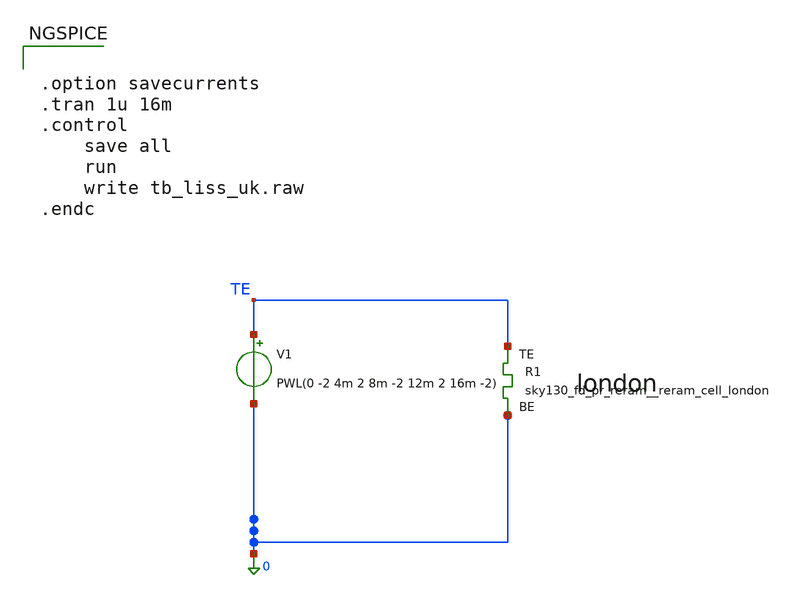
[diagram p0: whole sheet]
** sch_path: memristor_models/rram_london/tb_liss_uk.sch
**.subckt tb_liss_uk
V1 TE 0 PWL(0 -2 4m 2 8m -2 12m 2 16m -2)
XR1 TE 0 sky130_fd_pr_reram__reram_cell_london
**** begin user architecture code

** opencircuitdesign pdks install
.inc $::SKYWATER_MODELS/sky130_fd_pr_reram__reram_cell_london.spice



.option savecurrents
.tran 1u 16m
.control
	save all
	run
	write tb_liss_uk.raw
.endc



**** end user architecture code
**.ends
.end
